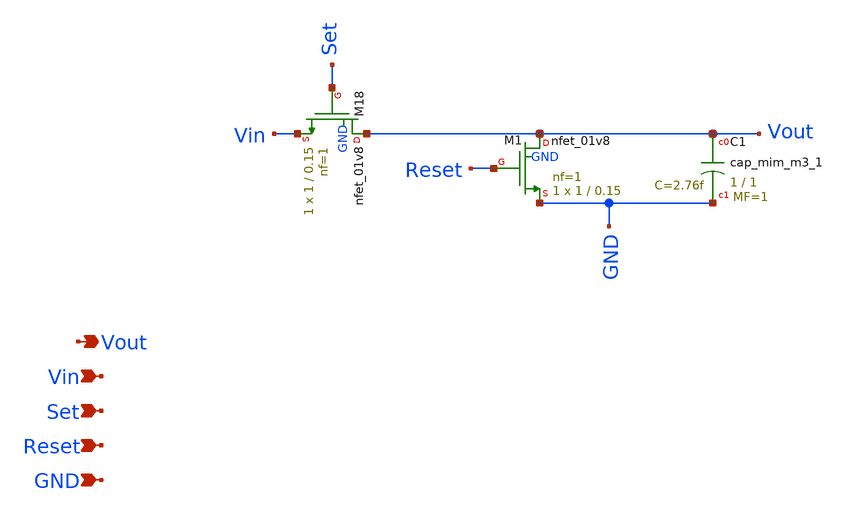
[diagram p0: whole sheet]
** sch_path: trackhold.sch
**.subckt trackhold Vout Vin Set Reset GND
*.opin Vout
*.ipin Vin
*.ipin Set
*.ipin Reset
*.ipin GND
XC1 Vout GND sky130_fd_pr__cap_mim_m3_1 W=1 L=1 MF=1 m=1
XM18 Vout Set Vin GND sky130_fd_pr__nfet_01v8 L=0.15 W=1 nf=1 ad='int((nf+1)/2) * W/nf * 0.29' as='int((nf+2)/2) * W/nf * 0.29'
+ pd='2*int((nf+1)/2) * (W/nf + 0.29)' ps='2*int((nf+2)/2) * (W/nf + 0.29)' nrd='0.29 / W' nrs='0.29 / W'
+ sa=0 sb=0 sd=0 mult=1 m=1
XM1 Vout Reset GND GND sky130_fd_pr__nfet_01v8 L=0.15 W=1 nf=1 ad='int((nf+1)/2) * W/nf * 0.29' as='int((nf+2)/2) * W/nf * 0.29'
+ pd='2*int((nf+1)/2) * (W/nf + 0.29)' ps='2*int((nf+2)/2) * (W/nf + 0.29)' nrd='0.29 / W' nrs='0.29 / W'
+ sa=0 sb=0 sd=0 mult=1 m=1
**.ends
.end
